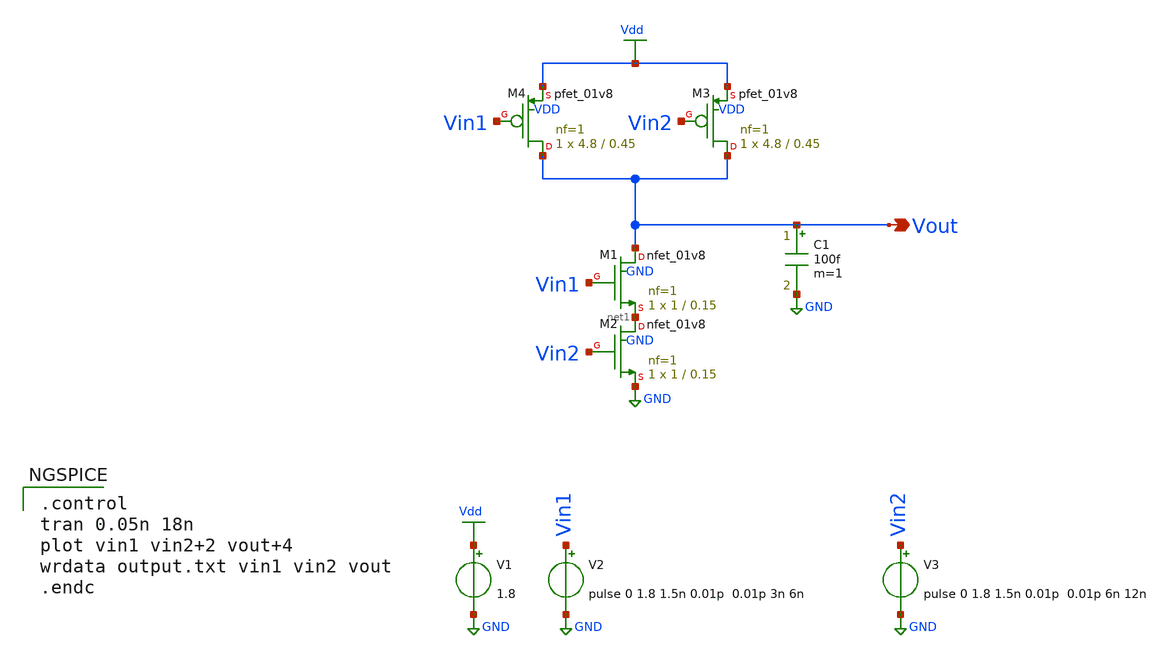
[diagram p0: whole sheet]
** sch_path: Circuiti/porta-nand.sch
**.subckt porta-nand Vout
*.opin Vout
XM1 Vout Vin1 net1 GND sky130_fd_pr__nfet_01v8 L=0.15 W=1 nf=1 ad='int((nf+1)/2) * W/nf * 0.29' as='int((nf+2)/2) * W/nf * 0.29'
+ pd='2*int((nf+1)/2) * (W/nf + 0.29)' ps='2*int((nf+2)/2) * (W/nf + 0.29)' nrd='0.29 / W' nrs='0.29 / W'
+ sa=0 sb=0 sd=0 mult=1 m=1
V1 Vdd GND 1.8
XM3 Vout Vin2 Vdd VDD sky130_fd_pr__pfet_01v8 L=0.45 W=4.8 nf=1 ad='int((nf+1)/2) * W/nf * 0.29' as='int((nf+2)/2) * W/nf * 0.29'
+ pd='2*int((nf+1)/2) * (W/nf + 0.29)' ps='2*int((nf+2)/2) * (W/nf + 0.29)' nrd='0.29 / W' nrs='0.29 / W'
+ sa=0 sb=0 sd=0 mult=1 m=1
V2 Vin1 GND pulse 0 1.8 1.5n 0.01p 0.01p 3n 6n
C1 Vout GND 100f m=1
XM4 Vout Vin1 Vdd VDD sky130_fd_pr__pfet_01v8 L=0.45 W=4.8 nf=1 ad='int((nf+1)/2) * W/nf * 0.29' as='int((nf+2)/2) * W/nf * 0.29'
+ pd='2*int((nf+1)/2) * (W/nf + 0.29)' ps='2*int((nf+2)/2) * (W/nf + 0.29)' nrd='0.29 / W' nrs='0.29 / W'
+ sa=0 sb=0 sd=0 mult=1 m=1
XM2 net1 Vin2 GND GND sky130_fd_pr__nfet_01v8 L=0.15 W=1 nf=1 ad='int((nf+1)/2) * W/nf * 0.29' as='int((nf+2)/2) * W/nf * 0.29'
+ pd='2*int((nf+1)/2) * (W/nf + 0.29)' ps='2*int((nf+2)/2) * (W/nf + 0.29)' nrd='0.29 / W' nrs='0.29 / W'
+ sa=0 sb=0 sd=0 mult=1 m=1
V3 Vin2 GND pulse 0 1.8 1.5n 0.01p 0.01p 6n 12n
**** begin user architecture code


.lib /home/matteo/xschem_downloads/skywater-pdk/libraries/sky130_fd_pr_ngspice/latest/models/sky130.lib.spice tt

*.include /home/matteo/xschem_downloads/skywater-pdk/libraries/sky130_fd_pr_ngspice/latest/cells/nfet_01v8/sky130_fd_pr__nfet_01v8__tt.corner.spice

.param mc_mm_switch=0
.param mc_pr_switch=1



.control
tran 0.05n 18n
plot vin1 vin2+2 vout+4
wrdata output.txt vin1 vin2 vout
.endc


**** end user architecture code
**.ends
.GLOBAL Vdd
.GLOBAL GND
.end
